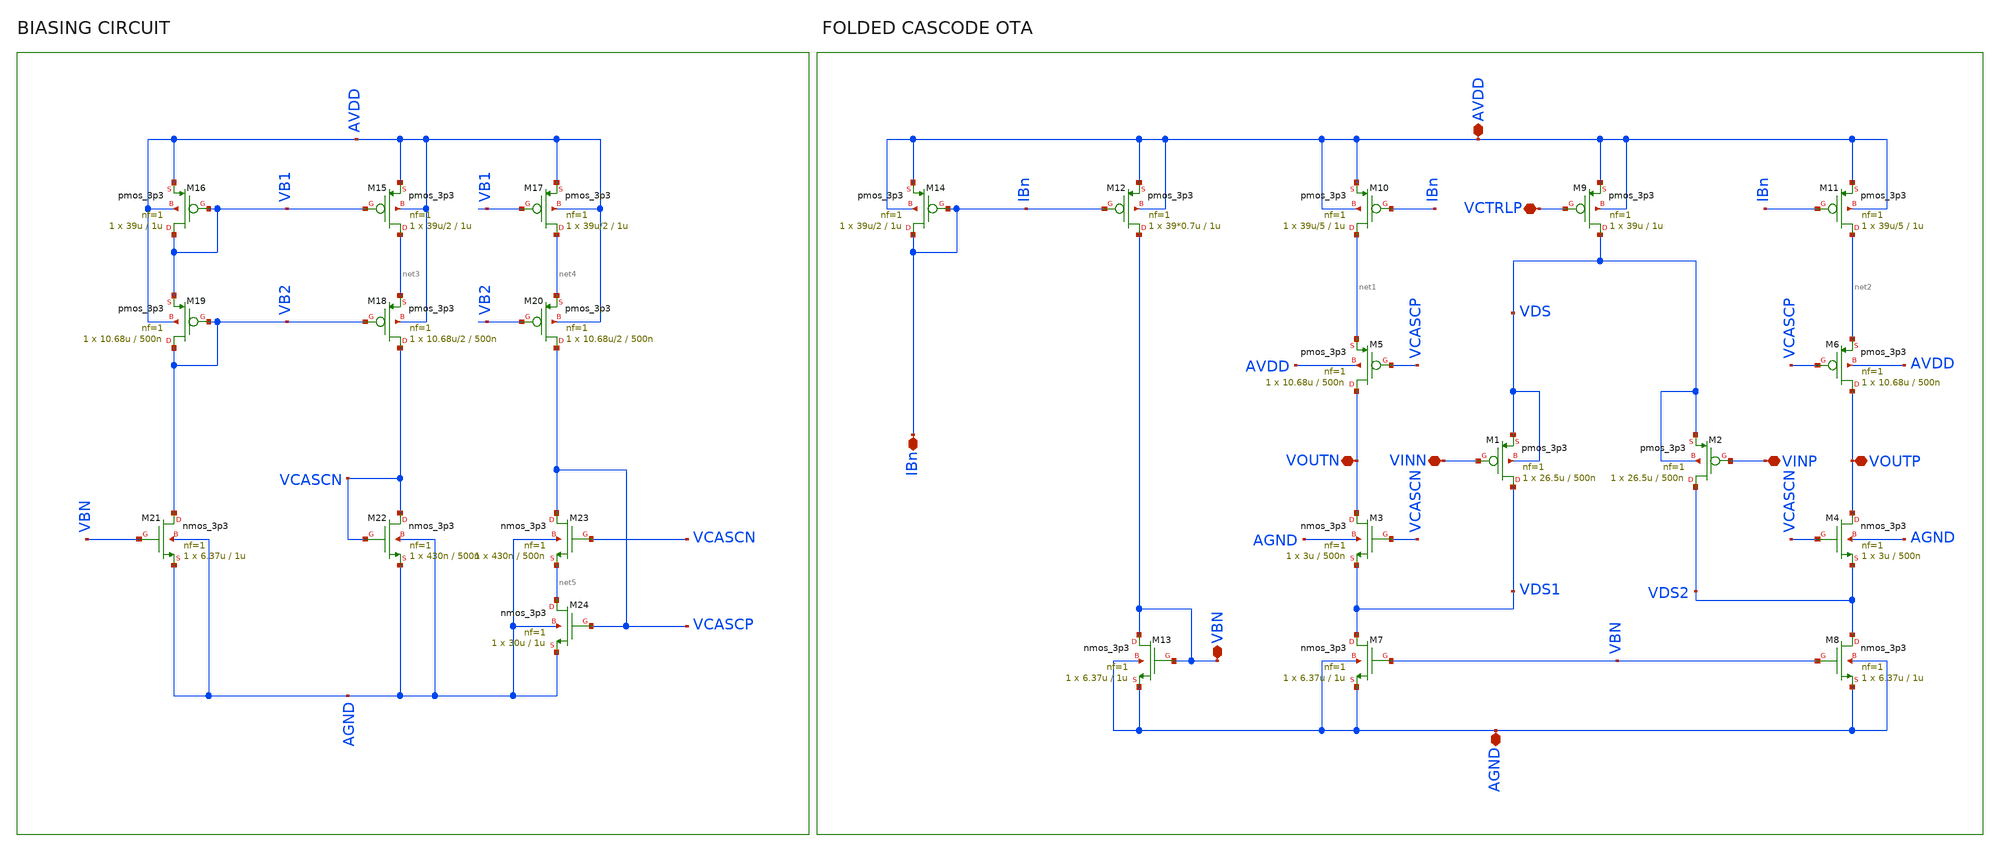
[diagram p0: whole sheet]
** sch_path: ITI_Labs/Lab11_Xschem/Design/OTA.sch
**.subckt OTA IBn AVDD AGND VINN VINP VOUTN VOUTP VCTRLP VBN
*.iopin IBn
*.iopin AVDD
*.iopin AGND
*.iopin VINN
*.iopin VINP
*.iopin VOUTN
*.iopin VOUTP
*.iopin VCTRLP
*.iopin VBN
XM2 VDS2 VINP VDS VDS pmos_3p3 L=500n W=26.5u nf=1 ad='int((nf+1)/2) * W/nf * 0.18u' as='int((nf+2)/2) * W/nf * 0.18u'
+ pd='2*int((nf+1)/2) * (W/nf + 0.18u)' ps='2*int((nf+2)/2) * (W/nf + 0.18u)' nrd='0.18u / W' nrs='0.18u / W'
+ sa=0 sb=0 sd=0 m=1
XM1 VDS1 VINN VDS VDS pmos_3p3 L=500n W=26.5u nf=1 ad='int((nf+1)/2) * W/nf * 0.18u' as='int((nf+2)/2) * W/nf * 0.18u'
+ pd='2*int((nf+1)/2) * (W/nf + 0.18u)' ps='2*int((nf+2)/2) * (W/nf + 0.18u)' nrd='0.18u / W' nrs='0.18u / W'
+ sa=0 sb=0 sd=0 m=1
XM9 VDS VCTRLP AVDD AVDD pmos_3p3 L=1u W=39u nf=1 ad='int((nf+1)/2) * W/nf * 0.18u' as='int((nf+2)/2) * W/nf * 0.18u'
+ pd='2*int((nf+1)/2) * (W/nf + 0.18u)' ps='2*int((nf+2)/2) * (W/nf + 0.18u)' nrd='0.18u / W' nrs='0.18u / W'
+ sa=0 sb=0 sd=0 m=1
XM6 VOUTP VCASCP net2 AVDD pmos_3p3 L=500n W=10.68u nf=1 ad='int((nf+1)/2) * W/nf * 0.18u' as='int((nf+2)/2) * W/nf * 0.18u'
+ pd='2*int((nf+1)/2) * (W/nf + 0.18u)' ps='2*int((nf+2)/2) * (W/nf + 0.18u)' nrd='0.18u / W' nrs='0.18u / W'
+ sa=0 sb=0 sd=0 m=1
XM11 net2 IBn AVDD AVDD pmos_3p3 L=1u W=39u/5 nf=1 ad='int((nf+1)/2) * W/nf * 0.18u' as='int((nf+2)/2) * W/nf * 0.18u'
+ pd='2*int((nf+1)/2) * (W/nf + 0.18u)' ps='2*int((nf+2)/2) * (W/nf + 0.18u)' nrd='0.18u / W' nrs='0.18u / W'
+ sa=0 sb=0 sd=0 m=1
XM4 VOUTP VCASCN VDS2 AGND nmos_3p3 L=500n W=3u nf=1 ad='int((nf+1)/2) * W/nf * 0.18u' as='int((nf+2)/2) * W/nf * 0.18u'
+ pd='2*int((nf+1)/2) * (W/nf + 0.18u)' ps='2*int((nf+2)/2) * (W/nf + 0.18u)' nrd='0.18u / W' nrs='0.18u / W'
+ sa=0 sb=0 sd=0 m=1
XM8 VDS2 VBN AGND AGND nmos_3p3 L=1u W=6.37u nf=1 ad='int((nf+1)/2) * W/nf * 0.18u' as='int((nf+2)/2) * W/nf * 0.18u'
+ pd='2*int((nf+1)/2) * (W/nf + 0.18u)' ps='2*int((nf+2)/2) * (W/nf + 0.18u)' nrd='0.18u / W' nrs='0.18u / W'
+ sa=0 sb=0 sd=0 m=1
XM5 VOUTN VCASCP net1 AVDD pmos_3p3 L=500n W=10.68u nf=1 ad='int((nf+1)/2) * W/nf * 0.18u' as='int((nf+2)/2) * W/nf * 0.18u'
+ pd='2*int((nf+1)/2) * (W/nf + 0.18u)' ps='2*int((nf+2)/2) * (W/nf + 0.18u)' nrd='0.18u / W' nrs='0.18u / W'
+ sa=0 sb=0 sd=0 m=1
XM10 net1 IBn AVDD AVDD pmos_3p3 L=1u W=39u/5 nf=1 ad='int((nf+1)/2) * W/nf * 0.18u' as='int((nf+2)/2) * W/nf * 0.18u'
+ pd='2*int((nf+1)/2) * (W/nf + 0.18u)' ps='2*int((nf+2)/2) * (W/nf + 0.18u)' nrd='0.18u / W' nrs='0.18u / W'
+ sa=0 sb=0 sd=0 m=1
XM3 VOUTN VCASCN VDS1 AGND nmos_3p3 L=500n W=3u nf=1 ad='int((nf+1)/2) * W/nf * 0.18u' as='int((nf+2)/2) * W/nf * 0.18u'
+ pd='2*int((nf+1)/2) * (W/nf + 0.18u)' ps='2*int((nf+2)/2) * (W/nf + 0.18u)' nrd='0.18u / W' nrs='0.18u / W'
+ sa=0 sb=0 sd=0 m=1
XM7 VDS1 VBN AGND AGND nmos_3p3 L=1u W=6.37u nf=1 ad='int((nf+1)/2) * W/nf * 0.18u' as='int((nf+2)/2) * W/nf * 0.18u'
+ pd='2*int((nf+1)/2) * (W/nf + 0.18u)' ps='2*int((nf+2)/2) * (W/nf + 0.18u)' nrd='0.18u / W' nrs='0.18u / W'
+ sa=0 sb=0 sd=0 m=1
XM12 VBN IBn AVDD AVDD pmos_3p3 L=1u W=39*0.7u nf=1 ad='int((nf+1)/2) * W/nf * 0.18u' as='int((nf+2)/2) * W/nf * 0.18u'
+ pd='2*int((nf+1)/2) * (W/nf + 0.18u)' ps='2*int((nf+2)/2) * (W/nf + 0.18u)' nrd='0.18u / W' nrs='0.18u / W'
+ sa=0 sb=0 sd=0 m=1
XM13 VBN VBN AGND AGND nmos_3p3 L=1u W=6.37u nf=1 ad='int((nf+1)/2) * W/nf * 0.18u' as='int((nf+2)/2) * W/nf * 0.18u'
+ pd='2*int((nf+1)/2) * (W/nf + 0.18u)' ps='2*int((nf+2)/2) * (W/nf + 0.18u)' nrd='0.18u / W' nrs='0.18u / W'
+ sa=0 sb=0 sd=0 m=1
XM14 IBn IBn AVDD AVDD pmos_3p3 L=1u W=39u/2 nf=1 ad='int((nf+1)/2) * W/nf * 0.18u' as='int((nf+2)/2) * W/nf * 0.18u'
+ pd='2*int((nf+1)/2) * (W/nf + 0.18u)' ps='2*int((nf+2)/2) * (W/nf + 0.18u)' nrd='0.18u / W' nrs='0.18u / W'
+ sa=0 sb=0 sd=0 m=1
XM15 net3 VB1 AVDD AVDD pmos_3p3 L=1u W=39u/2 nf=1 ad='int((nf+1)/2) * W/nf * 0.18u' as='int((nf+2)/2) * W/nf * 0.18u'
+ pd='2*int((nf+1)/2) * (W/nf + 0.18u)' ps='2*int((nf+2)/2) * (W/nf + 0.18u)' nrd='0.18u / W' nrs='0.18u / W'
+ sa=0 sb=0 sd=0 m=1
XM16 VB1 VB1 AVDD AVDD pmos_3p3 L=1u W=39u nf=1 ad='int((nf+1)/2) * W/nf * 0.18u' as='int((nf+2)/2) * W/nf * 0.18u'
+ pd='2*int((nf+1)/2) * (W/nf + 0.18u)' ps='2*int((nf+2)/2) * (W/nf + 0.18u)' nrd='0.18u / W' nrs='0.18u / W'
+ sa=0 sb=0 sd=0 m=1
XM17 net4 VB1 AVDD AVDD pmos_3p3 L=1u W=39u/2 nf=1 ad='int((nf+1)/2) * W/nf * 0.18u' as='int((nf+2)/2) * W/nf * 0.18u'
+ pd='2*int((nf+1)/2) * (W/nf + 0.18u)' ps='2*int((nf+2)/2) * (W/nf + 0.18u)' nrd='0.18u / W' nrs='0.18u / W'
+ sa=0 sb=0 sd=0 m=1
XM18 VCASCN VB2 net3 AVDD pmos_3p3 L=500n W=10.68u/2 nf=1 ad='int((nf+1)/2) * W/nf * 0.18u' as='int((nf+2)/2) * W/nf * 0.18u'
+ pd='2*int((nf+1)/2) * (W/nf + 0.18u)' ps='2*int((nf+2)/2) * (W/nf + 0.18u)' nrd='0.18u / W' nrs='0.18u / W'
+ sa=0 sb=0 sd=0 m=1
XM19 VB2 VB2 VB1 AVDD pmos_3p3 L=500n W=10.68u nf=1 ad='int((nf+1)/2) * W/nf * 0.18u' as='int((nf+2)/2) * W/nf * 0.18u'
+ pd='2*int((nf+1)/2) * (W/nf + 0.18u)' ps='2*int((nf+2)/2) * (W/nf + 0.18u)' nrd='0.18u / W' nrs='0.18u / W'
+ sa=0 sb=0 sd=0 m=1
XM20 VCASCP VB2 net4 AVDD pmos_3p3 L=500n W=10.68u/2 nf=1 ad='int((nf+1)/2) * W/nf * 0.18u' as='int((nf+2)/2) * W/nf * 0.18u'
+ pd='2*int((nf+1)/2) * (W/nf + 0.18u)' ps='2*int((nf+2)/2) * (W/nf + 0.18u)' nrd='0.18u / W' nrs='0.18u / W'
+ sa=0 sb=0 sd=0 m=1
XM21 VB2 VBN AGND AGND nmos_3p3 L=1u W=6.37u nf=1 ad='int((nf+1)/2) * W/nf * 0.18u' as='int((nf+2)/2) * W/nf * 0.18u'
+ pd='2*int((nf+1)/2) * (W/nf + 0.18u)' ps='2*int((nf+2)/2) * (W/nf + 0.18u)' nrd='0.18u / W' nrs='0.18u / W'
+ sa=0 sb=0 sd=0 m=1
XM22 VCASCN VCASCN AGND AGND nmos_3p3 L=500n W=430n nf=1 ad='int((nf+1)/2) * W/nf * 0.18u' as='int((nf+2)/2) * W/nf * 0.18u'
+ pd='2*int((nf+1)/2) * (W/nf + 0.18u)' ps='2*int((nf+2)/2) * (W/nf + 0.18u)' nrd='0.18u / W' nrs='0.18u / W'
+ sa=0 sb=0 sd=0 m=1
XM23 VCASCP VCASCN net5 AGND nmos_3p3 L=500n W=430n nf=1 ad='int((nf+1)/2) * W/nf * 0.18u' as='int((nf+2)/2) * W/nf * 0.18u'
+ pd='2*int((nf+1)/2) * (W/nf + 0.18u)' ps='2*int((nf+2)/2) * (W/nf + 0.18u)' nrd='0.18u / W' nrs='0.18u / W'
+ sa=0 sb=0 sd=0 m=1
XM24 net5 VCASCP AGND AGND nmos_3p3 L=1u W=30u nf=1 ad='int((nf+1)/2) * W/nf * 0.18u' as='int((nf+2)/2) * W/nf * 0.18u'
+ pd='2*int((nf+1)/2) * (W/nf + 0.18u)' ps='2*int((nf+2)/2) * (W/nf + 0.18u)' nrd='0.18u / W' nrs='0.18u / W'
+ sa=0 sb=0 sd=0 m=1
**** begin user architecture code


**** end user architecture code
**.ends
.end
